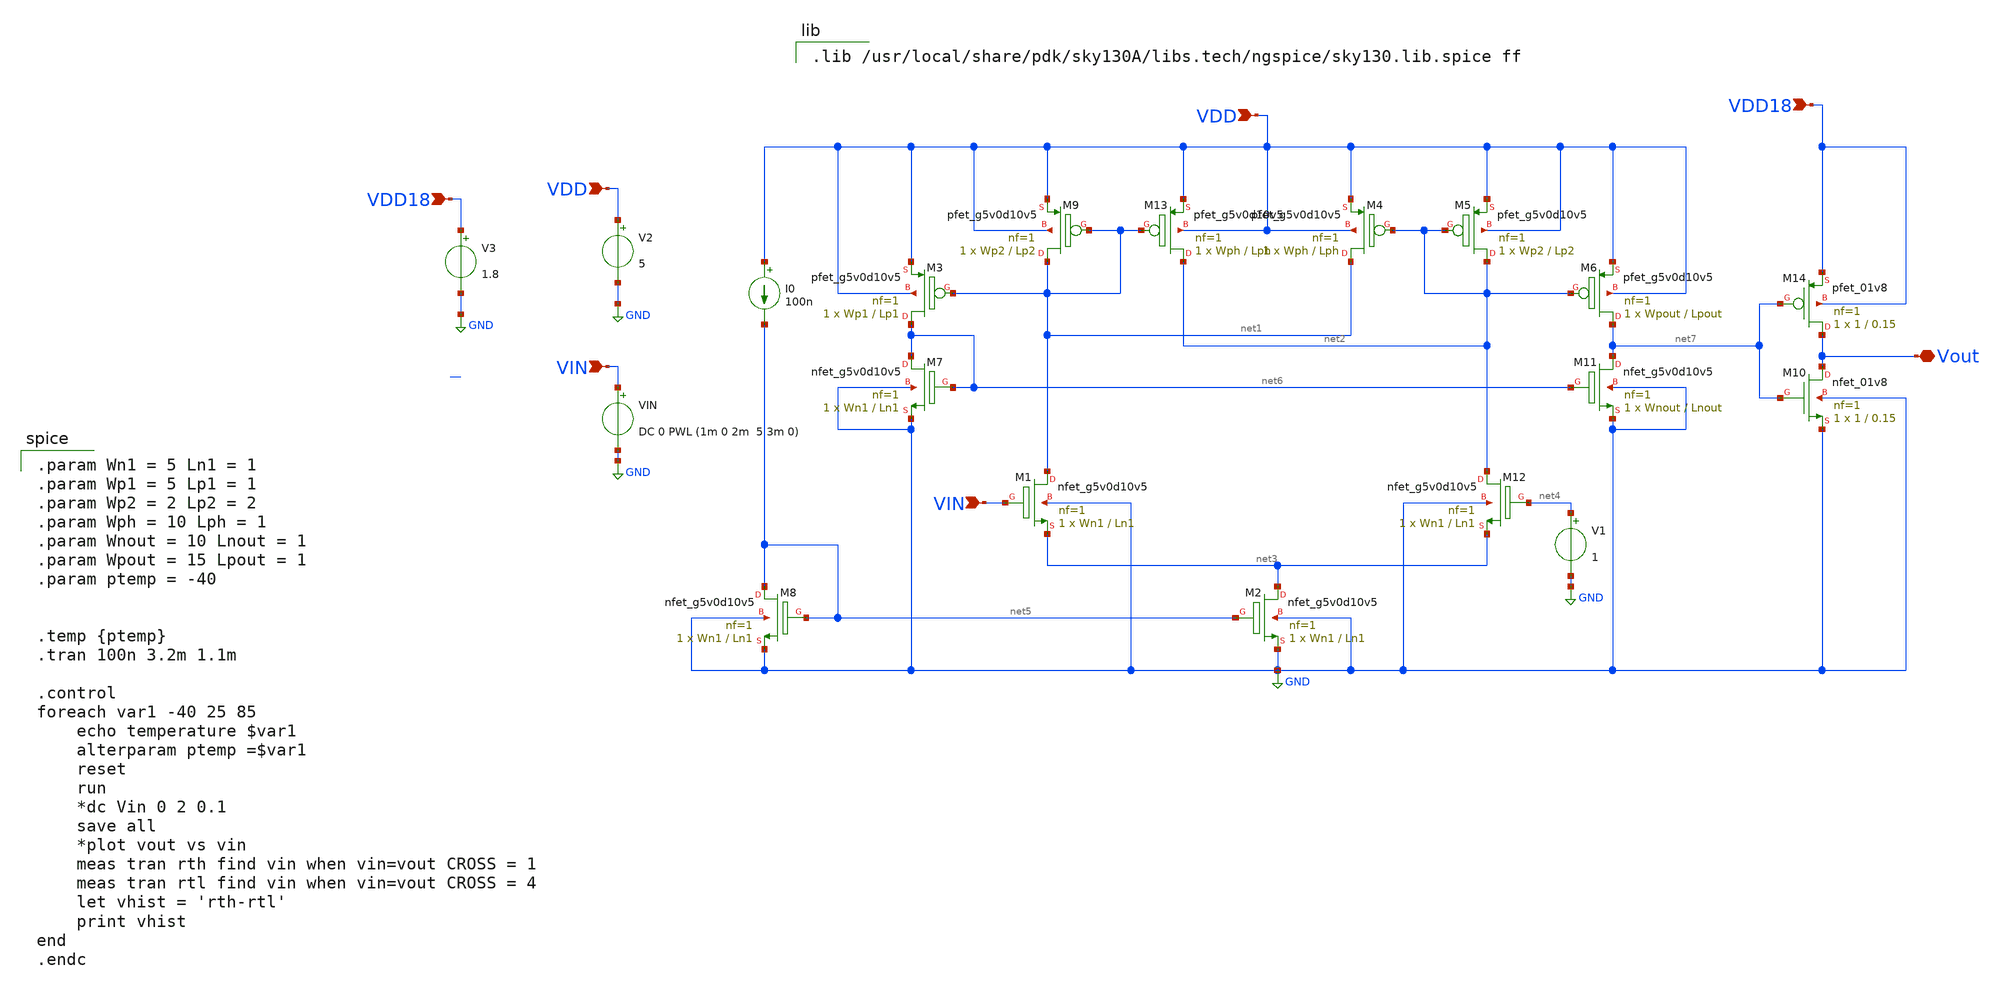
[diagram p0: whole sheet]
** sch_path: xschem/Comparador_completo_modificado.sch
**.subckt Comparador_completo_modificado VDD VDD Vout VIN VIN VDD18 VDD18
*.ipin VDD
*.ipin VDD
*.iopin Vout
*.ipin VIN
*.ipin VIN
*.ipin VDD18
*.ipin VDD18
V1 net4 GND 1
V2 VDD GND 5
VIN VIN GND DC 0 PWL (1m 0 2m 5 3m 0)
I0 VDD net5 100n
XM3 net6 net1 VDD VDD sky130_fd_pr__pfet_g5v0d10v5 L=Lp1 W=Wp1 nf=1 ad='int((nf+1)/2) * W/nf * 0.29'
+ as='int((nf+2)/2) * W/nf * 0.29' pd='2*int((nf+1)/2) * (W/nf + 0.29)' ps='2*int((nf+2)/2) * (W/nf + 0.29)'
+ nrd='0.29 / W' nrs='0.29 / W' sa=0 sb=0 sd=0 mult=1 m=1
XM9 net1 net1 VDD VDD sky130_fd_pr__pfet_g5v0d10v5 L=Lp2 W=Wp2 nf=1 ad='int((nf+1)/2) * W/nf * 0.29'
+ as='int((nf+2)/2) * W/nf * 0.29' pd='2*int((nf+1)/2) * (W/nf + 0.29)' ps='2*int((nf+2)/2) * (W/nf + 0.29)'
+ nrd='0.29 / W' nrs='0.29 / W' sa=0 sb=0 sd=0 mult=1 m=1
XM13 net2 net1 VDD VDD sky130_fd_pr__pfet_g5v0d10v5 L=Lph W=Wph nf=1 ad='int((nf+1)/2) * W/nf * 0.29'
+ as='int((nf+2)/2) * W/nf * 0.29' pd='2*int((nf+1)/2) * (W/nf + 0.29)' ps='2*int((nf+2)/2) * (W/nf + 0.29)'
+ nrd='0.29 / W' nrs='0.29 / W' sa=0 sb=0 sd=0 mult=1 m=1
XM4 net1 net2 VDD VDD sky130_fd_pr__pfet_g5v0d10v5 L=Lph W=Wph nf=1 ad='int((nf+1)/2) * W/nf * 0.29'
+ as='int((nf+2)/2) * W/nf * 0.29' pd='2*int((nf+1)/2) * (W/nf + 0.29)' ps='2*int((nf+2)/2) * (W/nf + 0.29)'
+ nrd='0.29 / W' nrs='0.29 / W' sa=0 sb=0 sd=0 mult=1 m=1
XM5 net2 net2 VDD VDD sky130_fd_pr__pfet_g5v0d10v5 L=Lp2 W=Wp2 nf=1 ad='int((nf+1)/2) * W/nf * 0.29'
+ as='int((nf+2)/2) * W/nf * 0.29' pd='2*int((nf+1)/2) * (W/nf + 0.29)' ps='2*int((nf+2)/2) * (W/nf + 0.29)'
+ nrd='0.29 / W' nrs='0.29 / W' sa=0 sb=0 sd=0 mult=1 m=1
XM6 net7 net2 VDD VDD sky130_fd_pr__pfet_g5v0d10v5 L=Lpout W=Wpout nf=1 ad='int((nf+1)/2) * W/nf * 0.29'
+ as='int((nf+2)/2) * W/nf * 0.29' pd='2*int((nf+1)/2) * (W/nf + 0.29)' ps='2*int((nf+2)/2) * (W/nf + 0.29)'
+ nrd='0.29 / W' nrs='0.29 / W' sa=0 sb=0 sd=0 mult=1 m=1
XM11 net7 net6 GND GND sky130_fd_pr__nfet_g5v0d10v5 L=Lnout W=Wnout nf=1 ad='int((nf+1)/2) * W/nf * 0.29'
+ as='int((nf+2)/2) * W/nf * 0.29' pd='2*int((nf+1)/2) * (W/nf + 0.29)' ps='2*int((nf+2)/2) * (W/nf + 0.29)'
+ nrd='0.29 / W' nrs='0.29 / W' sa=0 sb=0 sd=0 mult=1 m=1
XM12 net2 net4 net3 GND sky130_fd_pr__nfet_g5v0d10v5 L=Ln1 W=Wn1 nf=1 ad='int((nf+1)/2) * W/nf * 0.29'
+ as='int((nf+2)/2) * W/nf * 0.29' pd='2*int((nf+1)/2) * (W/nf + 0.29)' ps='2*int((nf+2)/2) * (W/nf + 0.29)'
+ nrd='0.29 / W' nrs='0.29 / W' sa=0 sb=0 sd=0 mult=1 m=1
XM2 net3 net5 GND GND sky130_fd_pr__nfet_g5v0d10v5 L=Ln1 W=Wn1 nf=1 ad='int((nf+1)/2) * W/nf * 0.29'
+ as='int((nf+2)/2) * W/nf * 0.29' pd='2*int((nf+1)/2) * (W/nf + 0.29)' ps='2*int((nf+2)/2) * (W/nf + 0.29)'
+ nrd='0.29 / W' nrs='0.29 / W' sa=0 sb=0 sd=0 mult=1 m=1
XM1 net1 VIN net3 GND sky130_fd_pr__nfet_g5v0d10v5 L=Ln1 W=Wn1 nf=1 ad='int((nf+1)/2) * W/nf * 0.29'
+ as='int((nf+2)/2) * W/nf * 0.29' pd='2*int((nf+1)/2) * (W/nf + 0.29)' ps='2*int((nf+2)/2) * (W/nf + 0.29)'
+ nrd='0.29 / W' nrs='0.29 / W' sa=0 sb=0 sd=0 mult=1 m=1
XM7 net6 net6 GND GND sky130_fd_pr__nfet_g5v0d10v5 L=Ln1 W=Wn1 nf=1 ad='int((nf+1)/2) * W/nf * 0.29'
+ as='int((nf+2)/2) * W/nf * 0.29' pd='2*int((nf+1)/2) * (W/nf + 0.29)' ps='2*int((nf+2)/2) * (W/nf + 0.29)'
+ nrd='0.29 / W' nrs='0.29 / W' sa=0 sb=0 sd=0 mult=1 m=1
XM8 net5 net5 GND GND sky130_fd_pr__nfet_g5v0d10v5 L=Ln1 W=Wn1 nf=1 ad='int((nf+1)/2) * W/nf * 0.29'
+ as='int((nf+2)/2) * W/nf * 0.29' pd='2*int((nf+1)/2) * (W/nf + 0.29)' ps='2*int((nf+2)/2) * (W/nf + 0.29)'
+ nrd='0.29 / W' nrs='0.29 / W' sa=0 sb=0 sd=0 mult=1 m=1
V3 VDD18 GND 1.8
XM10 Vout net7 GND GND sky130_fd_pr__nfet_01v8 L=0.15 W=1 nf=1 ad='int((nf+1)/2) * W/nf * 0.29' as='int((nf+2)/2) * W/nf * 0.29'
+ pd='2*int((nf+1)/2) * (W/nf + 0.29)' ps='2*int((nf+2)/2) * (W/nf + 0.29)' nrd='0.29 / W' nrs='0.29 / W'
+ sa=0 sb=0 sd=0 mult=1 m=1
XM14 Vout net7 VDD18 VDD18 sky130_fd_pr__pfet_01v8 L=0.15 W=1 nf=1 ad='int((nf+1)/2) * W/nf * 0.29' as='int((nf+2)/2) * W/nf * 0.29'
+ pd='2*int((nf+1)/2) * (W/nf + 0.29)' ps='2*int((nf+2)/2) * (W/nf + 0.29)' nrd='0.29 / W' nrs='0.29 / W'
+ sa=0 sb=0 sd=0 mult=1 m=1
**** begin user architecture code

.param Wn1 = 5 Ln1 = 1
.param Wp1 = 5 Lp1 = 1
.param Wp2 = 2 Lp2 = 2
.param Wph = 10 Lph = 1
.param Wnout = 10 Lnout = 1
.param Wpout = 15 Lpout = 1
.param ptemp = -40


.temp {ptemp}
.tran 100n 3.2m 1.1m

.control
foreach var1 -40 25 85
	echo temperature $var1
	alterparam ptemp =$var1
	reset
	run
	*dc Vin 0 2 0.1
	save all
	*plot vout vs vin
	meas tran rth find vin when vin=vout CROSS = 1
	meas tran rtl find vin when vin=vout CROSS = 4
	let vhist = 'rth-rtl'
	print vhist
end
.endc


.lib /usr/local/share/pdk/sky130A/libs.tech/ngspice/sky130.lib.spice ff

**** end user architecture code
**.ends
.GLOBAL GND
.end
